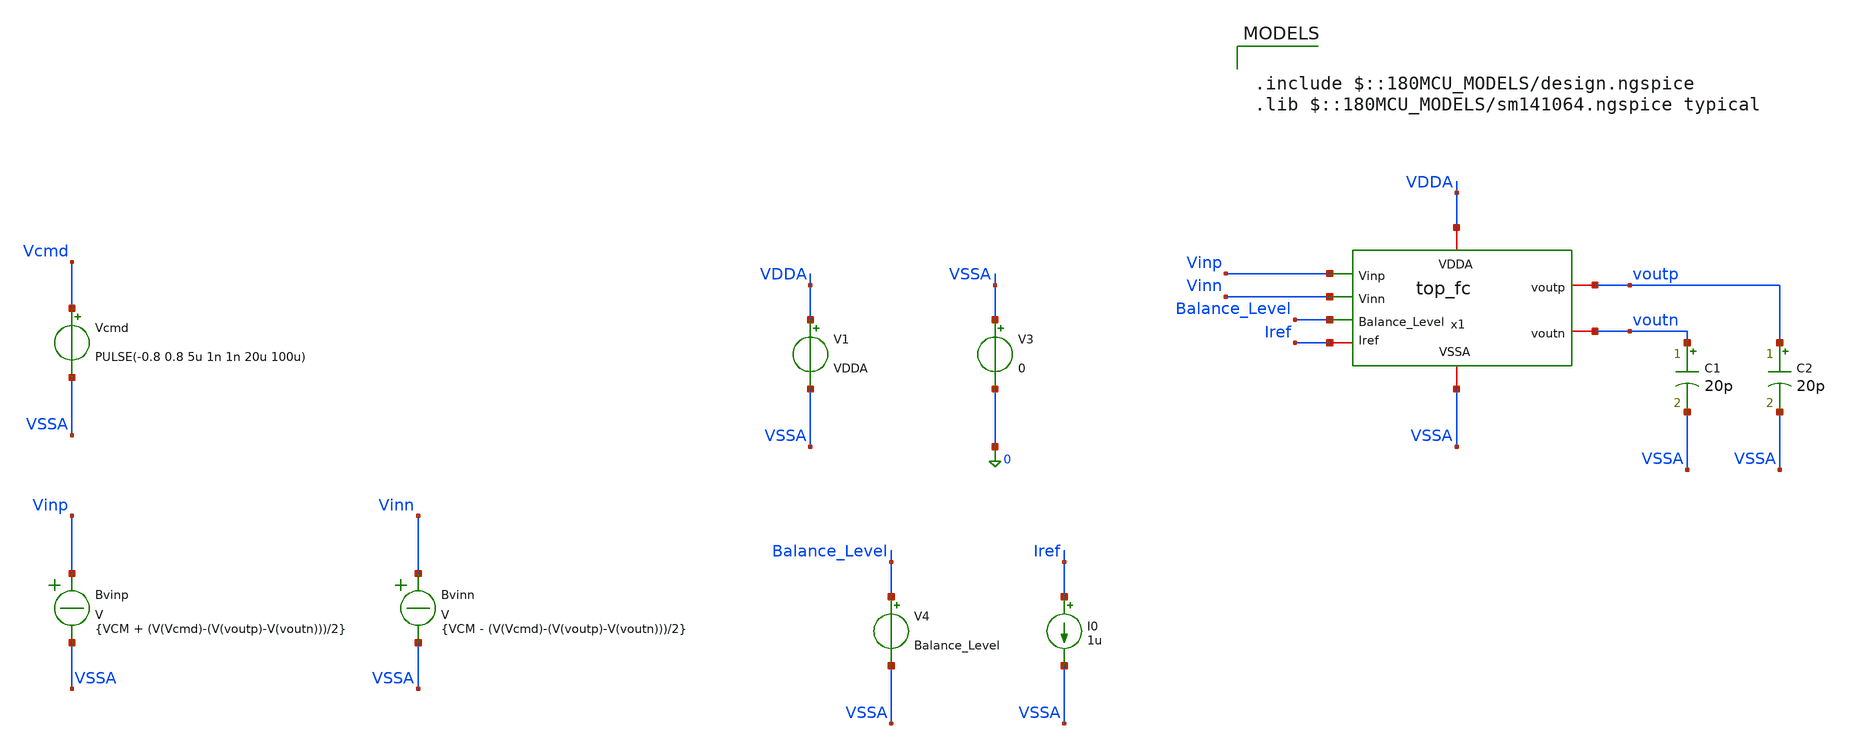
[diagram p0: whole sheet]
** sch_path: Folded_cascode/testbenches/top_fc_slew_rate_tb.sch
**.subckt top_fc_slew_rate_tb
x1 Balance_Level Vinp voutp VDDA voutn Vinn Iref VSSA top_fc
C1 voutn VSSA 20p m=1
C2 voutp VSSA 20p m=1
V1 VDDA VSSA VDDA
V3 VSSA 0 0
V4 Balance_Level VSSA Balance_Level
I0 Iref VSSA 1u
Bvinp Vinp VSSA V = {VCM + (V(Vcmd)-(V(voutp)-V(voutn)))/2}
Bvinn Vinn VSSA V = {VCM - (V(Vcmd)-(V(voutp)-V(voutn)))/2}
Vcmd Vcmd VSSA PULSE(-0.8 0.8 5u 1n 1n 20u 100u)
**** begin user architecture code

.include $::180MCU_MODELS/design.ngspice
.lib $::180MCU_MODELS/sm141064.ngspice typical



.temp 27
.param VDDA = 5
.param Balance_Level = 1.5
.param VD = 0
.param VCM = 2.5

.control
option sparse
set filetype=ascii
set wr_singlescale
set wr_vecnames
save all
save @m.x1.x1.xm1.m0[id]
save @m.x1.x1.xm1.m0[gm]
save @m.x1.x1.xm1.m0[vgs]
save @m.x1.x1.xm1.m0[vds]
save @m.x1.x1.xm1.m0[vth]
save @m.x1.x1.xm1.m0[gds]
save @m.x1.x1.xm1.m0[vdsat]

save @m.x1.x1.xm2.m0[id]
save @m.x1.x1.xm2.m0[gm]
save @m.x1.x1.xm2.m0[vgs]
save @m.x1.x1.xm2.m0[vds]
save @m.x1.x1.xm2.m0[vth]
save @m.x1.x1.xm2.m0[gds]
save @m.x1.x1.xm2.m0[vdsat]

save @m.x1.x1.xm9.m0[id]
save @m.x1.x1.xm9.m0[gm]
save @m.x1.x1.xm9.m0[vgs]
save @m.x1.x1.xm9.m0[vds]
save @m.x1.x1.xm9.m0[vth]
save @m.x1.x1.xm9.m0[gds]
save @m.x1.x1.xm9.m0[vdsat]

save @m.x1.x1.xm8.m0[id]
save @m.x1.x1.xm8.m0[gm]
save @m.x1.x1.xm8.m0[vgs]
save @m.x1.x1.xm8.m0[vds]
save @m.x1.x1.xm8.m0[vth]
save @m.x1.x1.xm8.m0[gds]
save @m.x1.x1.xm8.m0[vdsat]

save @m.x1.x1.xm6.m0[id]
save @m.x1.x1.xm6.m0[gm]
save @m.x1.x1.xm6.m0[vgs]
save @m.x1.x1.xm6.m0[vds]
save @m.x1.x1.xm6.m0[vth]
save @m.x1.x1.xm6.m0[gds]
save @m.x1.x1.xm6.m0[vdsat]

save @m.x1.x1.xm5.m0[id]
save @m.x1.x1.xm5.m0[gm]
save @m.x1.x1.xm5.m0[vgs]
save @m.x1.x1.xm5.m0[vds]
save @m.x1.x1.xm5.m0[vth]
save @m.x1.x1.xm5.m0[gds]
save @m.x1.x1.xm5.m0[vdsat]

save @m.x1.x2.xm1.m0[id]
save @m.x1.x2.xm1.m0[gm]
save @m.x1.x2.xm1.m0[vgs]
save @m.x1.x2.xm1.m0[vds]
save @m.x1.x2.xm1.m0[vth]
save @m.x1.x2.xm1.m0[gds]

save @m.x1.x2.xm2.m0[id]
save @m.x1.x2.xm2.m0[gm]
save @m.x1.x2.xm2.m0[vgs]
save @m.x1.x2.xm2.m0[vds]
save @m.x1.x2.xm2.m0[vth]
save @m.x1.x2.xm2.m0[gds]

save @m.x1.x2.xm3.m0[id]
save @m.x1.x2.xm3.m0[gm]
save @m.x1.x2.xm3.m0[vgs]
save @m.x1.x2.xm3.m0[vds]
save @m.x1.x2.xm3.m0[vth]
save @m.x1.x2.xm3.m0[gds]

save @m.x1.x2.xm4.m0[id]
save @m.x1.x2.xm4.m0[gm]
save @m.x1.x2.xm4.m0[vgs]
save @m.x1.x2.xm4.m0[vds]
save @m.x1.x2.xm4.m0[vth]
save @m.x1.x2.xm4.m0[gds]

save @m.x1.x2.xm5.m0[id]
save @m.x1.x2.xm5.m0[gm]
save @m.x1.x2.xm5.m0[vgs]
save @m.x1.x2.xm5.m0[vds]
save @m.x1.x2.xm5.m0[vth]
save @m.x1.x2.xm5.m0[gds]

save @m.x1.x2.xm6.m0[id]
save @m.x1.x2.xm6.m0[gm]
save @m.x1.x2.xm6.m0[vgs]
save @m.x1.x2.xm6.m0[vds]
save @m.x1.x2.xm6.m0[vth]
save @m.x1.x2.xm6.m0[gds]

save @m.x1.x2.xm7.m0[id]
save @m.x1.x2.xm7.m0[gm]
save @m.x1.x2.xm7.m0[vgs]
save @m.x1.x2.xm7.m0[vds]
save @m.x1.x2.xm7.m0[vth]
save @m.x1.x2.xm7.m0[gds]

save @m.x1.x2.xm8.m0[id]
save @m.x1.x2.xm8.m0[gm]
save @m.x1.x2.xm8.m0[vgs]
save @m.x1.x2.xm8.m0[vds]
save @m.x1.x2.xm8.m0[vth]
save @m.x1.x2.xm8.m0[gds]

save @m.x1.x2.xm9.m0[id]
save @m.x1.x2.xm9.m0[gm]
save @m.x1.x2.xm9.m0[vgs]
save @m.x1.x2.xm9.m0[vds]
save @m.x1.x2.xm9.m0[vth]
save @m.x1.x2.xm9.m0[gds]

save @m.x1.x3.xm1.m0[id]
save @m.x1.x3.xm1.m0[gm]
save @m.x1.x3.xm1.m0[vgs]
save @m.x1.x3.xm1.m0[vds]
save @m.x1.x3.xm1.m0[vth]
save @m.x1.x3.xm1.m0[gds]

save @m.x1.x3.xm2.m0[id]
save @m.x1.x3.xm2.m0[gm]
save @m.x1.x3.xm2.m0[vgs]
save @m.x1.x3.xm2.m0[vds]
save @m.x1.x3.xm2.m0[vth]
save @m.x1.x3.xm2.m0[gds]

save @m.x1.x3.xm3.m0[id]
save @m.x1.x3.xm3.m0[gm]
save @m.x1.x3.xm3.m0[vgs]
save @m.x1.x3.xm3.m0[vds]
save @m.x1.x3.xm3.m0[vth]
save @m.x1.x3.xm3.m0[gds]

save @m.x1.x3.xm4.m0[id]
save @m.x1.x3.xm4.m0[gm]
save @m.x1.x3.xm4.m0[vgs]
save @m.x1.x3.xm4.m0[vds]
save @m.x1.x3.xm4.m0[vth]
save @m.x1.x3.xm4.m0[gds]

save @m.x1.x3.xm5.m0[id]
save @m.x1.x3.xm5.m0[gm]
save @m.x1.x3.xm5.m0[vgs]
save @m.x1.x3.xm5.m0[vds]
save @m.x1.x3.xm5.m0[vth]
save @m.x1.x3.xm5.m0[gds]

save @m.x1.x3.xm6.m0[id]
save @m.x1.x3.xm6.m0[gm]
save @m.x1.x3.xm6.m0[vgs]
save @m.x1.x3.xm6.m0[vds]
save @m.x1.x3.xm6.m0[vth]
save @m.x1.x3.xm6.m0[gds]

save @m.x1.x3.xm7.m0[id]
save @m.x1.x3.xm7.m0[gm]
save @m.x1.x3.xm7.m0[vgs]
save @m.x1.x3.xm7.m0[vds]
save @m.x1.x3.xm7.m0[vth]
save @m.x1.x3.xm7.m0[gds]

save @m.x1.x3.xm8.m0[id]
save @m.x1.x3.xm8.m0[gm]
save @m.x1.x3.xm8.m0[vgs]
save @m.x1.x3.xm8.m0[vds]
save @m.x1.x3.xm8.m0[vth]
save @m.x1.x3.xm8.m0[gds]

save @m.x1.x3.xm9.m0[id]
save @m.x1.x3.xm9.m0[gm]
save @m.x1.x3.xm9.m0[vgs]
save @m.x1.x3.xm9.m0[vds]
save @m.x1.x3.xm9.m0[vth]
save @m.x1.x3.xm9.m0[gds]

save @m.x1.x3.xm10.m0[id]
save @m.x1.x3.xm10.m0[gm]
save @m.x1.x3.xm10.m0[vgs]
save @m.x1.x3.xm10.m0[vds]
save @m.x1.x3.xm10.m0[vth]
save @m.x1.x3.xm10.m0[gds]

save @m.x1.x3.xm11.m0[id]
save @m.x1.x3.xm11.m0[gm]
save @m.x1.x3.xm11.m0[vgs]
save @m.x1.x3.xm11.m0[vds]
save @m.x1.x3.xm11.m0[vth]
save @m.x1.x3.xm11.m0[gds]

save @m.x1.x3.xm12.m0[id]
save @m.x1.x3.xm12.m0[gm]
save @m.x1.x3.xm12.m0[vgs]
save @m.x1.x3.xm12.m0[vds]
save @m.x1.x3.xm12.m0[vth]
save @m.x1.x3.xm12.m0[gds]

save @m.x1.x3.xm13.m0[id]
save @m.x1.x3.xm13.m0[gm]
save @m.x1.x3.xm13.m0[vgs]
save @m.x1.x3.xm13.m0[vds]
save @m.x1.x3.xm13.m0[vth]
save @m.x1.x3.xm13.m0[gds]

save @m.x1.x3.xm14.m0[id]
save @m.x1.x3.xm14.m0[gm]
save @m.x1.x3.xm14.m0[vgs]
save @m.x1.x3.xm14.m0[vds]
save @m.x1.x3.xm14.m0[vth]
save @m.x1.x3.xm14.m0[gds]

save @m.x1.x3.xm15.m0[id]
save @m.x1.x3.xm15.m0[gm]
save @m.x1.x3.xm15.m0[vgs]
save @m.x1.x3.xm15.m0[vds]
save @m.x1.x3.xm15.m0[vth]
save @m.x1.x3.xm15.m0[gds]

save @m.x1.x3.xm16.m0[id]
save @m.x1.x3.xm16.m0[gm]
save @m.x1.x3.xm16.m0[vgs]
save @m.x1.x3.xm16.m0[vds]
save @m.x1.x3.xm16.m0[vth]
save @m.x1.x3.xm16.m0[gds]

save @m.x1.x3.xm17.m0[id]
save @m.x1.x3.xm17.m0[gm]
save @m.x1.x3.xm17.m0[vgs]
save @m.x1.x3.xm17.m0[vds]
save @m.x1.x3.xm17.m0[vth]
save @m.x1.x3.xm17.m0[gds]

save @m.x1.x3.xm18.m0[id]
save @m.x1.x3.xm18.m0[gm]
save @m.x1.x3.xm18.m0[vgs]
save @m.x1.x3.xm18.m0[vds]
save @m.x1.x3.xm18.m0[vth]
save @m.x1.x3.xm18.m0[gds]

save @m.x1.x3.xm21.m0[id]
save @m.x1.x3.xm21.m0[gm]
save @m.x1.x3.xm21.m0[vgs]
save @m.x1.x3.xm21.m0[vds]
save @m.x1.x3.xm21.m0[vth]
save @m.x1.x3.xm21.m0[gds]

save @m.x1.x3.xm22.m0[id]
save @m.x1.x3.xm22.m0[gm]
save @m.x1.x3.xm22.m0[vgs]
save @m.x1.x3.xm22.m0[vds]
save @m.x1.x3.xm22.m0[vth]
save @m.x1.x3.xm22.m0[gds]

op
write top_fc_op_tb.raw all

* ============================================================
* TRANSIENT
* ============================================================

tran 10n 45u


* ============================================================
* OUTPUT QUANTITIES
* ============================================================

let vod  = v(voutp)-v(voutn)
let vocm = (v(voutp)+v(voutn))/2

let dvod_dt = deriv(vod)


* ============================================================
* PEAK INSTANTANEOUS SLEW RATE
* ============================================================

meas tran sr_pos MAX dvod_dt
meas tran sr_neg MIN dvod_dt

let sr_pos_vus = sr_pos*1e-6
let sr_neg_vus = abs(sr_neg)*1e-6

print sr_pos_vus
print sr_neg_vus


* ============================================================
* 10%-90% RISING SLEW RATE
*
* Step:
*   -0.8 V -> +0.8 V
*
* 10% = -0.64 V
* 90% = +0.64 V
*
* Delta Vod = 1.28 V
* ============================================================

meas tran t_rise_10 WHEN vod=-0.64 RISE=1
meas tran t_rise_90 WHEN vod=0.64 RISE=1

let tr_10_90 = t_rise_90-t_rise_10

let sr_rise_10_90 = 1.28/tr_10_90
let sr_rise_10_90_vus = sr_rise_10_90*1e-6

print t_rise_10
print t_rise_90
print tr_10_90
print sr_rise_10_90_vus


* ============================================================
* 90%-10% FALLING SLEW RATE
* ============================================================

meas tran t_fall_90 WHEN vod=0.64 FALL=1
meas tran t_fall_10 WHEN vod=-0.64 FALL=1

let tf_90_10 = t_fall_10-t_fall_90

let sr_fall_90_10 = 1.28/tf_90_10
let sr_fall_90_10_vus = sr_fall_90_10*1e-6

print t_fall_90
print t_fall_10
print tf_90_10
print sr_fall_90_10_vus


* ============================================================
* SAVE
* ============================================================

write top_fc_slew_rate_tb.raw


* ============================================================
* PLOTS
* ============================================================

plot v(Vcmd) vod
plot v(voutp) v(voutn)
plot vocm
plot dvod_dt*1e-6

.endc


**** end user architecture code
**.ends
.end
